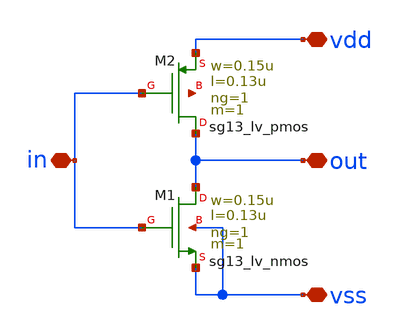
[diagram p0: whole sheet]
** sch_path: design/blocks/inverter/inverter.sch
**.subckt inverter out vdd vss in
*.iopin out
*.iopin vdd
*.iopin vss
*.iopin in
XM1 out in vss vss sg13_lv_nmos w=0.15u l=0.13u ng=1 m=1 mm_ok=1
XM2 out in vdd net1 sg13_lv_pmos w=0.15u l=0.13u ng=1 m=1 mm_ok=1
**.ends
.end
